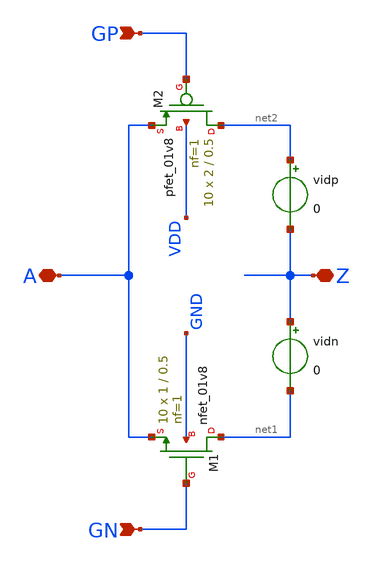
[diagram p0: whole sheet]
** sch_path: dacpassgate.sch
* Copyright 2021 Stefan Frederik Schippers
* Licensed under the Apache License, Version 2.0 (the "License");
* you may not use this file except in compliance with the License.
* You may obtain a copy of the License at
* https://www.apache.org/licenses/LICENSE-2.0
* Unless required by applicable law or agreed to in writing, software
* distributed under the License is distributed on an "AS IS" BASIS,
* WITHOUT WARRANTIES OR CONDITIONS OF ANY KIND, either express or implied.
* See the License for the specific language governing permissions and
* limitations under the License.
**.subckt dacpassgate A Z GP GN
*.iopin A
*.iopin Z
*.ipin GP
*.ipin GN
XM1 net1 GN A GND sky130_fd_pr__nfet_01v8 L=0.5 W=1 nf=1 ad='int((nf+1)/2) * W/nf * 0.29' as='int((nf+2)/2) * W/nf * 0.29'
+ pd='2*int((nf+1)/2) * (W/nf + 0.29)' ps='2*int((nf+2)/2) * (W/nf + 0.29)' nrd='0.29 / W' nrs='0.29 / W'
+ sa=0 sb=0 sd=0 mult=10 m=10
XM2 net2 GP A VDD sky130_fd_pr__pfet_01v8 L=0.5 W=2 nf=1 ad='int((nf+1)/2) * W/nf * 0.29' as='int((nf+2)/2) * W/nf * 0.29'
+ pd='2*int((nf+1)/2) * (W/nf + 0.29)' ps='2*int((nf+2)/2) * (W/nf + 0.29)' nrd='0.29 / W' nrs='0.29 / W'
+ sa=0 sb=0 sd=0 mult=10 m=10
vidp net2 Z 0
vidn Z net1 0
**.ends
.end
